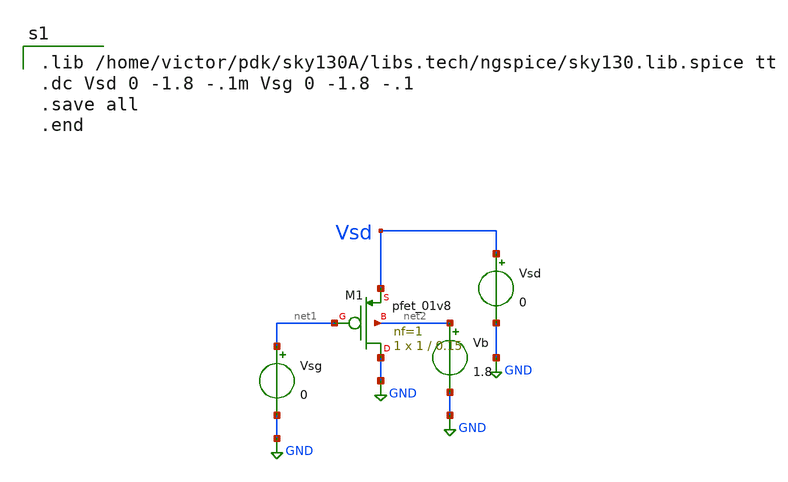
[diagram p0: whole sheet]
** sch_path: Schematics/PMOSIVCharacteristics.sch
**.subckt PMOSIVCharacteristics
XM1 GND net1 Vsd net2 sky130_fd_pr__pfet_01v8 L=0.15 W=1 nf=1 ad='int((nf+1)/2) * W/nf * 0.29' as='int((nf+2)/2) * W/nf * 0.29'
+ pd='2*int((nf+1)/2) * (W/nf + 0.29)' ps='2*int((nf+2)/2) * (W/nf + 0.29)' nrd='0.29 / W' nrs='0.29 / W'
+ sa=0 sb=0 sd=0 mult=1 m=1
Vsg net1 GND 0
Vsd Vsd GND 0
Vb net2 GND 1.8
**** begin user architecture code

.lib /home/victor/pdk/sky130A/libs.tech/ngspice/sky130.lib.spice tt
.dc Vsd 0 -1.8 -.1m Vsg 0 -1.8 -.1
.save all
.end

**** end user architecture code
**.ends
.GLOBAL GND
.end
